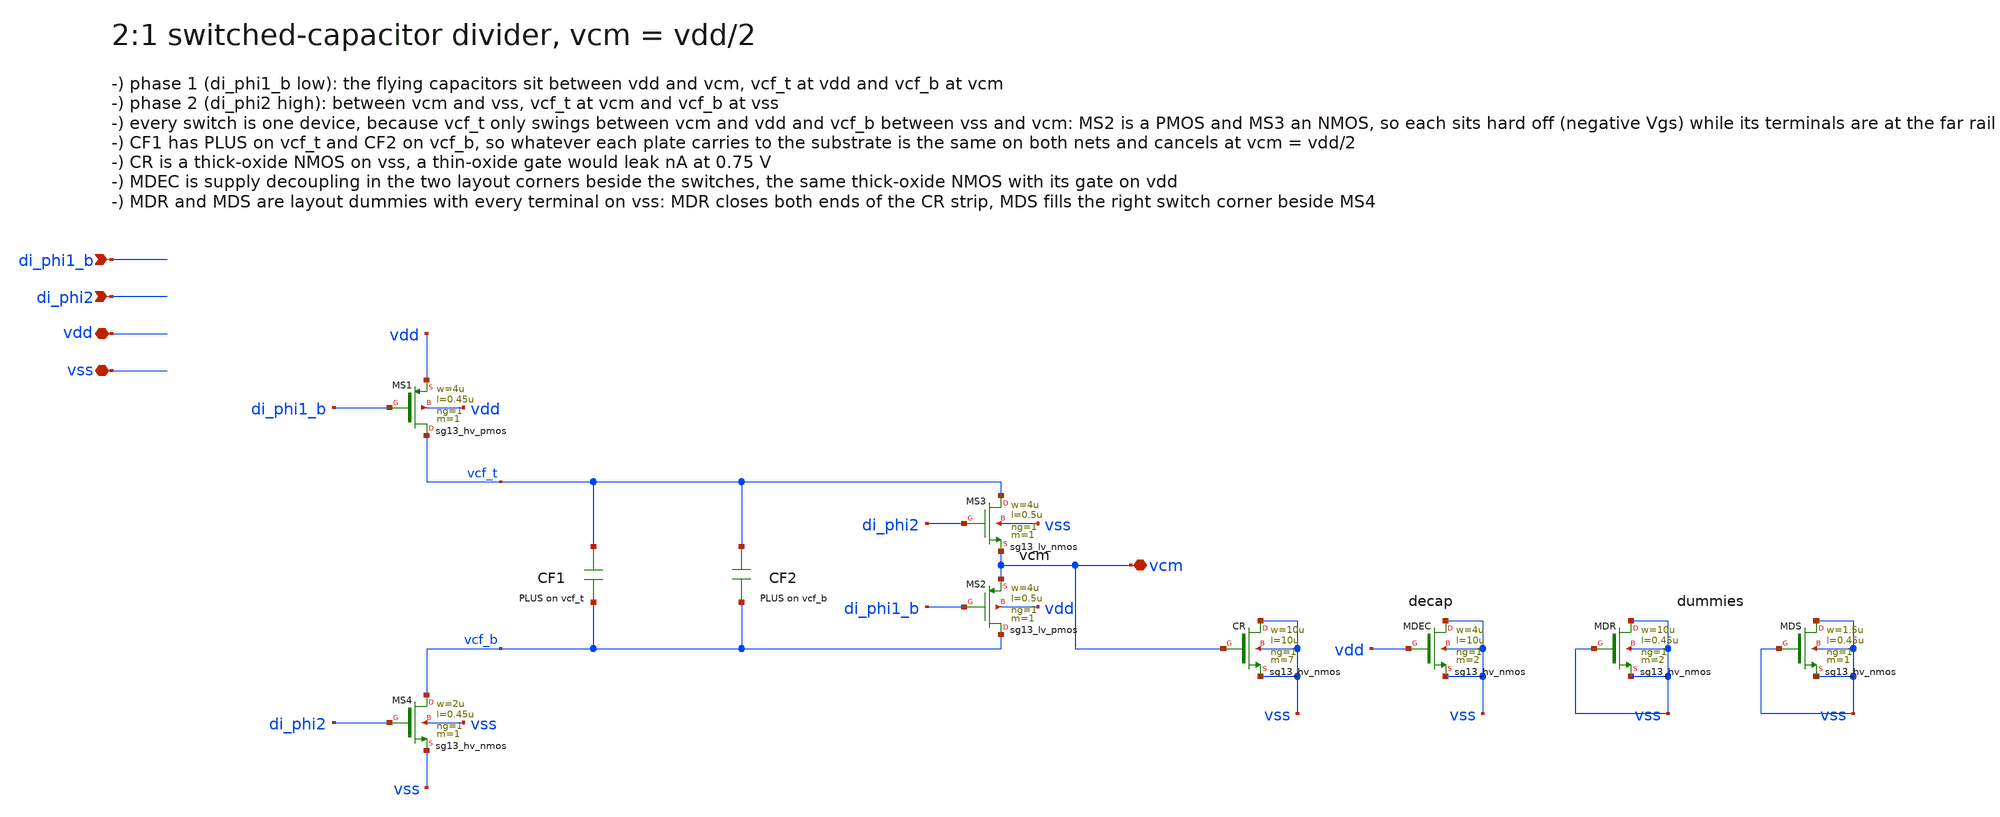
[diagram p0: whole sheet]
** sch_path: ip/dsm2_core/schematic/vcm_gen.sch
* (c) 2026 Michael Koefinger
**.subckt vcm_gen di_phi1_b di_phi2 vdd vss vcm
*.ipin di_phi1_b
*.ipin di_phi2
*.iopin vdd
*.iopin vss
*.iopin vcm
XMS1 vcf_t di_phi1_b vdd vdd sg13_hv_pmos w=4u l=0.45u ng=1 m=1 mm_ok=1
XMS4 vcf_b di_phi2 vss vss sg13_hv_nmos w=2u l=0.45u ng=1 m=1 mm_ok=1
XMS2 vcf_b di_phi1_b vcm vdd sg13_lv_pmos w=4u l=0.5u ng=1 m=1 mm_ok=1
XMS3 vcf_t di_phi2 vcm vss sg13_lv_nmos w=4u l=0.5u ng=1 m=1 mm_ok=1
XCF1[3] vcf_t vcf_b cap_cmomf w=4.2e-6 l=12.4e-6 mmin=3 mmax=4 subblock=0 m=1 mm_ok=1
XCF1[2] vcf_t vcf_b cap_cmomf w=4.2e-6 l=12.4e-6 mmin=3 mmax=4 subblock=0 m=1 mm_ok=1
XCF1[1] vcf_t vcf_b cap_cmomf w=4.2e-6 l=12.4e-6 mmin=3 mmax=4 subblock=0 m=1 mm_ok=1
XCF1[0] vcf_t vcf_b cap_cmomf w=4.2e-6 l=12.4e-6 mmin=3 mmax=4 subblock=0 m=1 mm_ok=1
XCF2[3] vcf_b vcf_t cap_cmomf w=4.2e-6 l=12.4e-6 mmin=3 mmax=4 subblock=0 m=1 mm_ok=1
XCF2[2] vcf_b vcf_t cap_cmomf w=4.2e-6 l=12.4e-6 mmin=3 mmax=4 subblock=0 m=1 mm_ok=1
XCF2[1] vcf_b vcf_t cap_cmomf w=4.2e-6 l=12.4e-6 mmin=3 mmax=4 subblock=0 m=1 mm_ok=1
XCF2[0] vcf_b vcf_t cap_cmomf w=4.2e-6 l=12.4e-6 mmin=3 mmax=4 subblock=0 m=1 mm_ok=1
XCR vss vcm vss vss sg13_hv_nmos w=10u l=10u ng=1 m=7 mm_ok=1
XMDEC vss vdd vss vss sg13_hv_nmos w=4u l=10u ng=1 m=2 mm_ok=1
XMDR vss vss vss vss sg13_hv_nmos w=10u l=0.45u ng=1 m=2 mm_ok=1
XMDS vss vss vss vss sg13_hv_nmos w=1.5u l=0.45u ng=1 m=1 mm_ok=1
**.ends
.end
